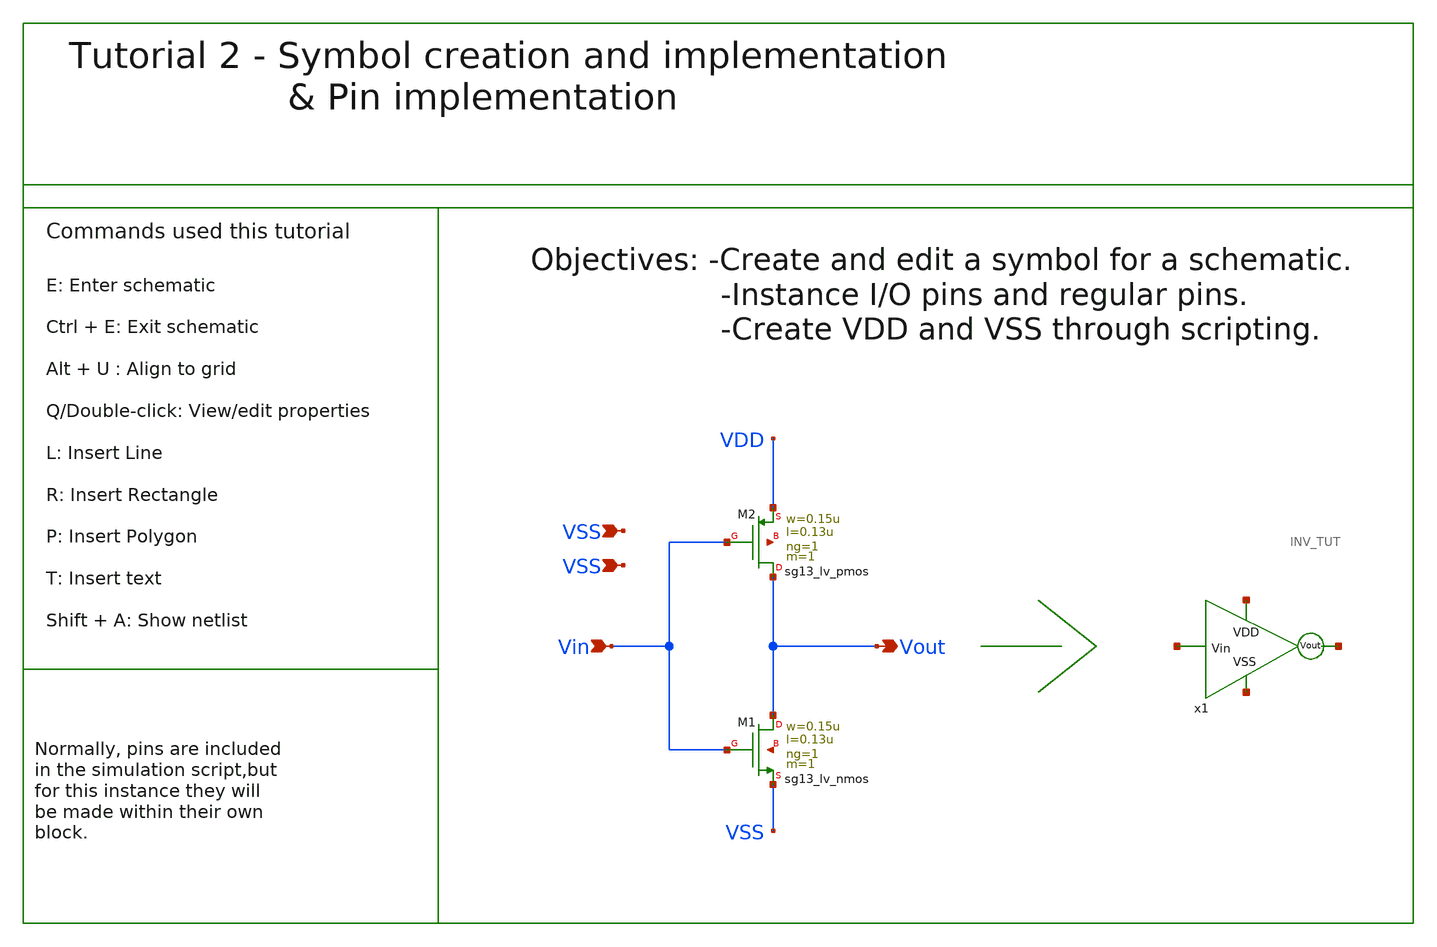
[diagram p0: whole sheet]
** sch_path: Tutoriales/Tutorial_2.sch
**.subckt Tutorial_2 Vin Vout VSS VSS
*.ipin Vin
*.opin Vout
*.ipin VSS
*.ipin VSS
XM1 Vout Vin VSS net1 sg13_lv_nmos w=0.15u l=0.13u ng=1 m=1 mm_ok=1
XM2 Vout Vin VDD net2 sg13_lv_pmos w=0.15u l=0.13u ng=1 m=1 mm_ok=1
x1 net3 net4 net5 net6 INV_TUT
**** begin user architecture code



vvdd vdd 0 dc 1.8
vvss vss 0 0

* SYNTAX: Name of source  ,  Node where voltage is applied  , Negative port ,   type of source  ,
*+ positive port
* These are instances of two voltage sources with a GND point of reference

.end


**** end user architecture code
**.ends

* expanding   symbol:  /foss/designs/Tutoriales_Xschem/Tutoriales/INV_TUT.sym # of pins=4
** sym_path: Tutoriales/INV_TUT.sym
** sch_path: Tutoriales/INV_TUT.sch
.subckt INV_TUT VSS VDD Vout Vin
*.ipin Vin
*.opin Vout
*.ipin VSS
*.ipin VDD
XM1 Vout Vin VSS net1 sg13_lv_nmos w=0.15u l=0.13u ng=1 m=1 mm_ok=1
XM2 Vout Vin VDD net2 sg13_lv_pmos w=0.45u l=0.13u ng=1 m=1 mm_ok=1
.ends

.end
